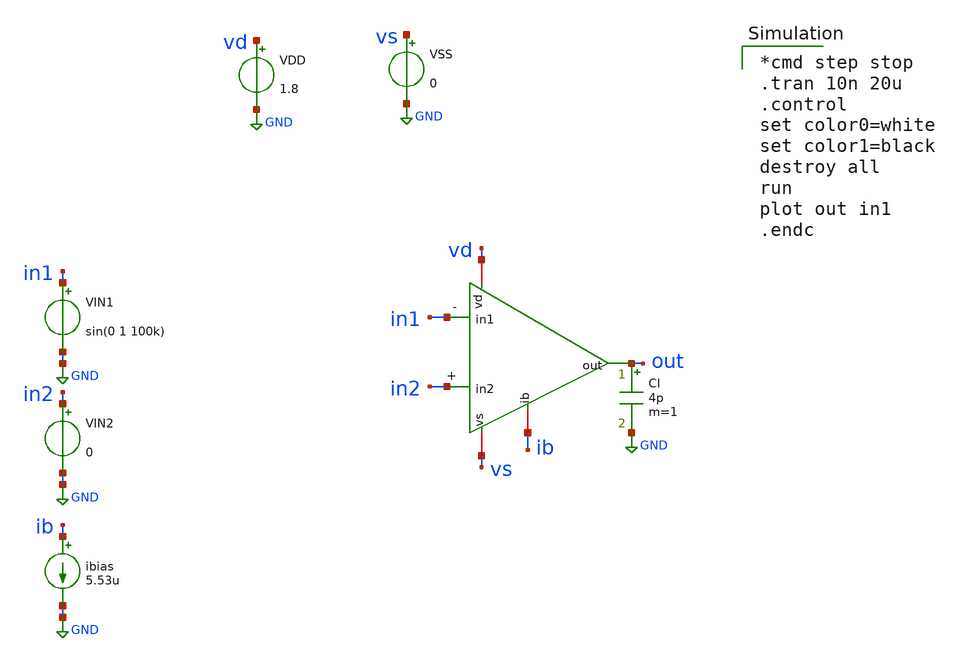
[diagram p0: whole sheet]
** sch_path: amp-op/xschem/ampop_tb-tran.sch
* Copyright 2020 Stefan Frederik Schippers
* Licensed under the Apache License, Version 2.0 (the "License");
* you may not use this file except in compliance with the License.
* You may obtain a copy of the License at
* https://www.apache.org/licenses/LICENSE-2.0
* Unless required by applicable law or agreed to in writing, software
* distributed under the License is distributed on an "AS IS" BASIS,
* WITHOUT WARRANTIES OR CONDITIONS OF ANY KIND, either express or implied.
* See the License for the specific language governing permissions and
* limitations under the License.
**.subckt ampop_tb-tran
VIN2 in2 GND 0
VIN1 in1 GND sin(0 1 100k)
ibias ib GND 5.53u
VDD vd GND 1.8
VSS vs GND 0
Cl out GND 4p m=1
x1 vd in1 in2 out ib vs ampop
**** begin user architecture code

*cmd step stop
.tran 10n 20u
.control
set color0=white
set color1=black
destroy all
run
plot out in1
.endc

 .lib $::SKYWATER_MODELS/sky130.lib.spice tt
.include $::SKYWATER_STDCELLS/sky130_fd_sc_hd.spice

**** end user architecture code
**.ends
.GLOBAL GND
.end
